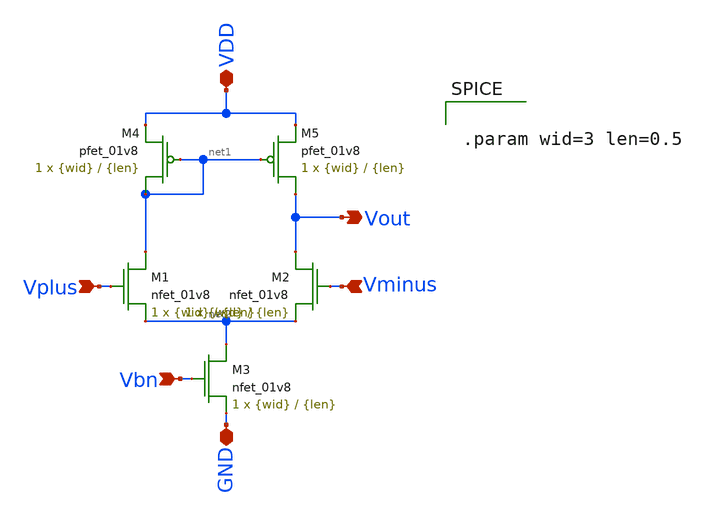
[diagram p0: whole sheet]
** sch_path: final/schematics/opamp.sch
**.subckt opamp VDD GND Vplus Vminus Vout Vbn
*.iopin VDD
*.iopin GND
*.ipin Vplus
*.ipin Vminus
*.opin Vout
*.ipin Vbn
XM3 net2 Vbn GND GND sky130_fd_pr__nfet_01v8 L={len} W={wid} nf=1 ad='int((nf+1)/2) * W/nf * 0.29' as='int((nf+2)/2) * W/nf * 0.29'
+ pd='2*int((nf+1)/2) * (W/nf + 0.29)' ps='2*int((nf+2)/2) * (W/nf + 0.29)' nrd='0.29 / W' nrs='0.29 / W'
+ sa=0 sb=0 sd=0 mult=1 m=1
XM4 net1 net1 VDD VDD sky130_fd_pr__pfet_01v8 L={len} W={wid} nf=1 ad='int((nf+1)/2) * W/nf * 0.29' as='int((nf+2)/2) * W/nf * 0.29'
+ pd='2*int((nf+1)/2) * (W/nf + 0.29)' ps='2*int((nf+2)/2) * (W/nf + 0.29)' nrd='0.29 / W' nrs='0.29 / W'
+ sa=0 sb=0 sd=0 mult=1 m=1
XM5 Vout net1 VDD VDD sky130_fd_pr__pfet_01v8 L={len} W={wid} nf=1 ad='int((nf+1)/2) * W/nf * 0.29' as='int((nf+2)/2) * W/nf * 0.29'
+ pd='2*int((nf+1)/2) * (W/nf + 0.29)' ps='2*int((nf+2)/2) * (W/nf + 0.29)' nrd='0.29 / W' nrs='0.29 / W'
+ sa=0 sb=0 sd=0 mult=1 m=1
XM1 net1 Vplus net2 GND sky130_fd_pr__nfet_01v8 L={len} W={wid} nf=1 ad='int((nf+1)/2) * W/nf * 0.29'
+ as='int((nf+2)/2) * W/nf * 0.29' pd='2*int((nf+1)/2) * (W/nf + 0.29)' ps='2*int((nf+2)/2) * (W/nf + 0.29)'
+ nrd='0.29 / W' nrs='0.29 / W' sa=0 sb=0 sd=0 mult=1 m=1
XM2 Vout Vminus net2 GND sky130_fd_pr__nfet_01v8 L={len} W={wid} nf=1 ad='int((nf+1)/2) * W/nf * 0.29'
+ as='int((nf+2)/2) * W/nf * 0.29' pd='2*int((nf+1)/2) * (W/nf + 0.29)' ps='2*int((nf+2)/2) * (W/nf + 0.29)'
+ nrd='0.29 / W' nrs='0.29 / W' sa=0 sb=0 sd=0 mult=1 m=1
**** begin user architecture code


.param wid=3 len=0.5


**** end user architecture code
**.ends
.end
